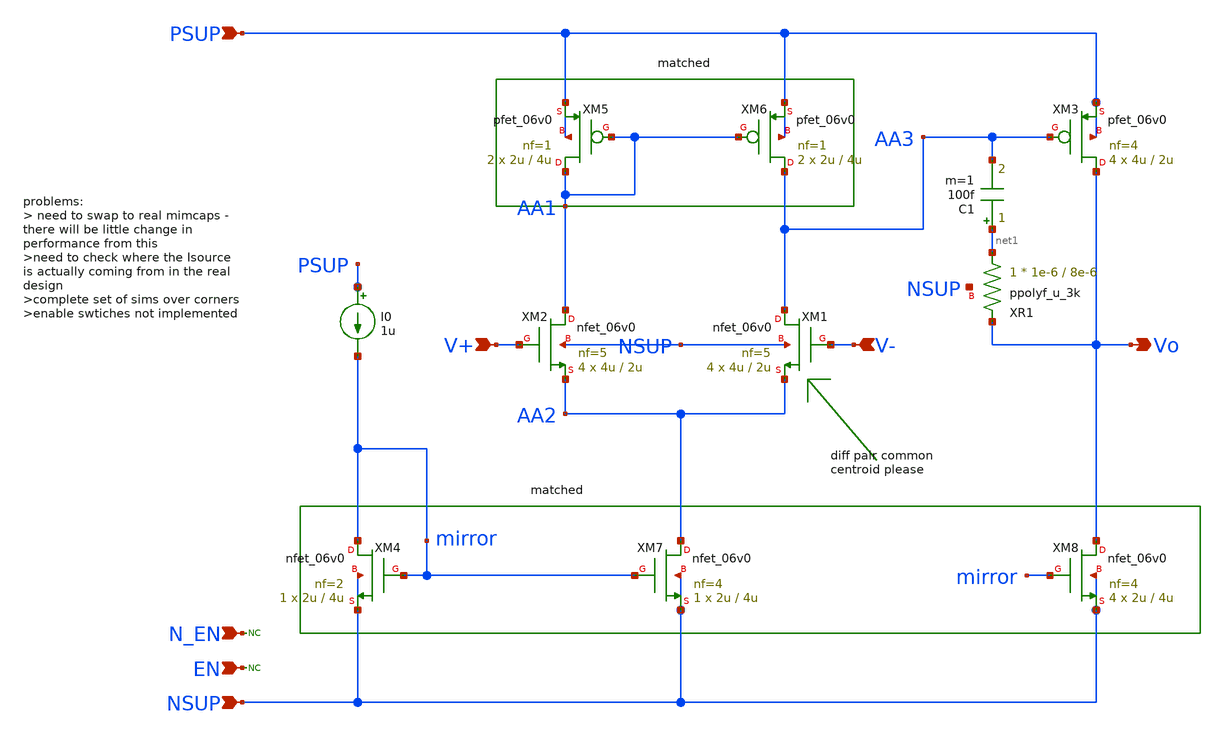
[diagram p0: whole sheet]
** sch_path: xschem/blocks/aux_amp/aux_amp.sch
**.subckt aux_amp PSUP NSUP N_EN EN V+ V- Vo
*.ipin PSUP
*.ipin NSUP
*.ipin N_EN
*.ipin EN
*.ipin V+
*.ipin V-
*.opin Vo
XM5 AA1 AA1 PSUP PSUP pfet_06v0 L=4u W=2u nf=1 ad='int((nf+1)/2) * W/nf * 0.18u' as='int((nf+2)/2) * W/nf * 0.18u'
+ pd='2*int((nf+1)/2) * (W/nf + 0.18u)' ps='2*int((nf+2)/2) * (W/nf + 0.18u)' nrd='0.18u / W' nrs='0.18u / W'
+ sa=0 sb=0 sd=0 m=2
XM6 AA3 AA1 PSUP PSUP pfet_06v0 L=4u W=2u nf=1 ad='int((nf+1)/2) * W/nf * 0.18u' as='int((nf+2)/2) * W/nf * 0.18u'
+ pd='2*int((nf+1)/2) * (W/nf + 0.18u)' ps='2*int((nf+2)/2) * (W/nf + 0.18u)' nrd='0.18u / W' nrs='0.18u / W'
+ sa=0 sb=0 sd=0 m=2
* noconn N_EN
* noconn EN
XM1 AA3 V- AA2 NSUP nfet_06v0 L=2u W=4u nf=5 ad='int((nf+1)/2) * W/nf * 0.18u' as='int((nf+2)/2) * W/nf * 0.18u'
+ pd='2*int((nf+1)/2) * (W/nf + 0.18u)' ps='2*int((nf+2)/2) * (W/nf + 0.18u)' nrd='0.18u / W' nrs='0.18u / W'
+ sa=0 sb=0 sd=0 m=4
XM2 AA1 V+ AA2 NSUP nfet_06v0 L=2u W=4u nf=5 ad='int((nf+1)/2) * W/nf * 0.18u' as='int((nf+2)/2) * W/nf * 0.18u'
+ pd='2*int((nf+1)/2) * (W/nf + 0.18u)' ps='2*int((nf+2)/2) * (W/nf + 0.18u)' nrd='0.18u / W' nrs='0.18u / W'
+ sa=0 sb=0 sd=0 m=4
C1 net1 AA3 100f m=1
XM4 mirror mirror NSUP NSUP nfet_06v0 L=4u W=2u nf=2 ad='int((nf+1)/2) * W/nf * 0.18u' as='int((nf+2)/2) * W/nf * 0.18u'
+ pd='2*int((nf+1)/2) * (W/nf + 0.18u)' ps='2*int((nf+2)/2) * (W/nf + 0.18u)' nrd='0.18u / W' nrs='0.18u / W'
+ sa=0 sb=0 sd=0 m=1
I0 PSUP mirror 1u
XM7 AA2 mirror NSUP NSUP nfet_06v0 L=4u W=2u nf=4 ad='int((nf+1)/2) * W/nf * 0.18u' as='int((nf+2)/2) * W/nf * 0.18u'
+ pd='2*int((nf+1)/2) * (W/nf + 0.18u)' ps='2*int((nf+2)/2) * (W/nf + 0.18u)' nrd='0.18u / W' nrs='0.18u / W'
+ sa=0 sb=0 sd=0 m=1
XM3 Vo AA3 PSUP PSUP pfet_06v0 L=2u W=4u nf=4 ad='int((nf+1)/2) * W/nf * 0.18u' as='int((nf+2)/2) * W/nf * 0.18u'
+ pd='2*int((nf+1)/2) * (W/nf + 0.18u)' ps='2*int((nf+2)/2) * (W/nf + 0.18u)' nrd='0.18u / W' nrs='0.18u / W'
+ sa=0 sb=0 sd=0 m=4
XM8 Vo mirror NSUP NSUP nfet_06v0 L=4u W=2u nf=4 ad='int((nf+1)/2) * W/nf * 0.18u' as='int((nf+2)/2) * W/nf * 0.18u'
+ pd='2*int((nf+1)/2) * (W/nf + 0.18u)' ps='2*int((nf+2)/2) * (W/nf + 0.18u)' nrd='0.18u / W' nrs='0.18u / W'
+ sa=0 sb=0 sd=0 m=4
XR1 net1 Vo NSUP ppolyf_u_3k r_width=1e-6 r_length=8e-6 m=1
**.ends
.end
